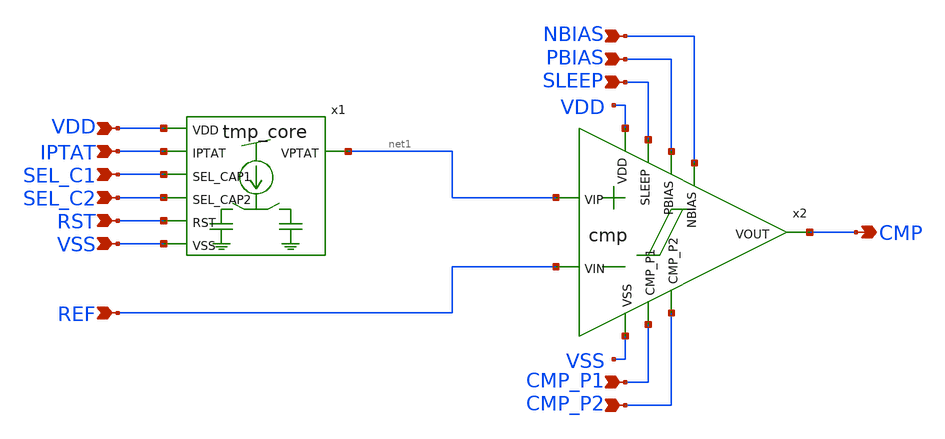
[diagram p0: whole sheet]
** sch_path: design/LELO_TORD_SKY130A/TB_tmp_core_and_cmp.sch
**.subckt TB_tmp_core_and_cmp VDD IPTAT SEL_C1 SEL_C2 RST VSS REF CMP SLEEP PBIAS NBIAS CMP_P1
*+ CMP_P2
*.ipin VDD
*.ipin IPTAT
*.ipin SEL_C1
*.ipin SEL_C2
*.ipin RST
*.ipin VSS
*.ipin REF
*.opin CMP
*.ipin SLEEP
*.ipin PBIAS
*.ipin NBIAS
*.ipin CMP_P1
*.ipin CMP_P2
x1 VDD IPTAT SEL_C1 SEL_C2 net1 RST VSS tmp_core
x2 NBIAS PBIAS CMP_P1 CMP_P2 SLEEP VDD net1 REF CMP VSS cmp
**.ends
.end
